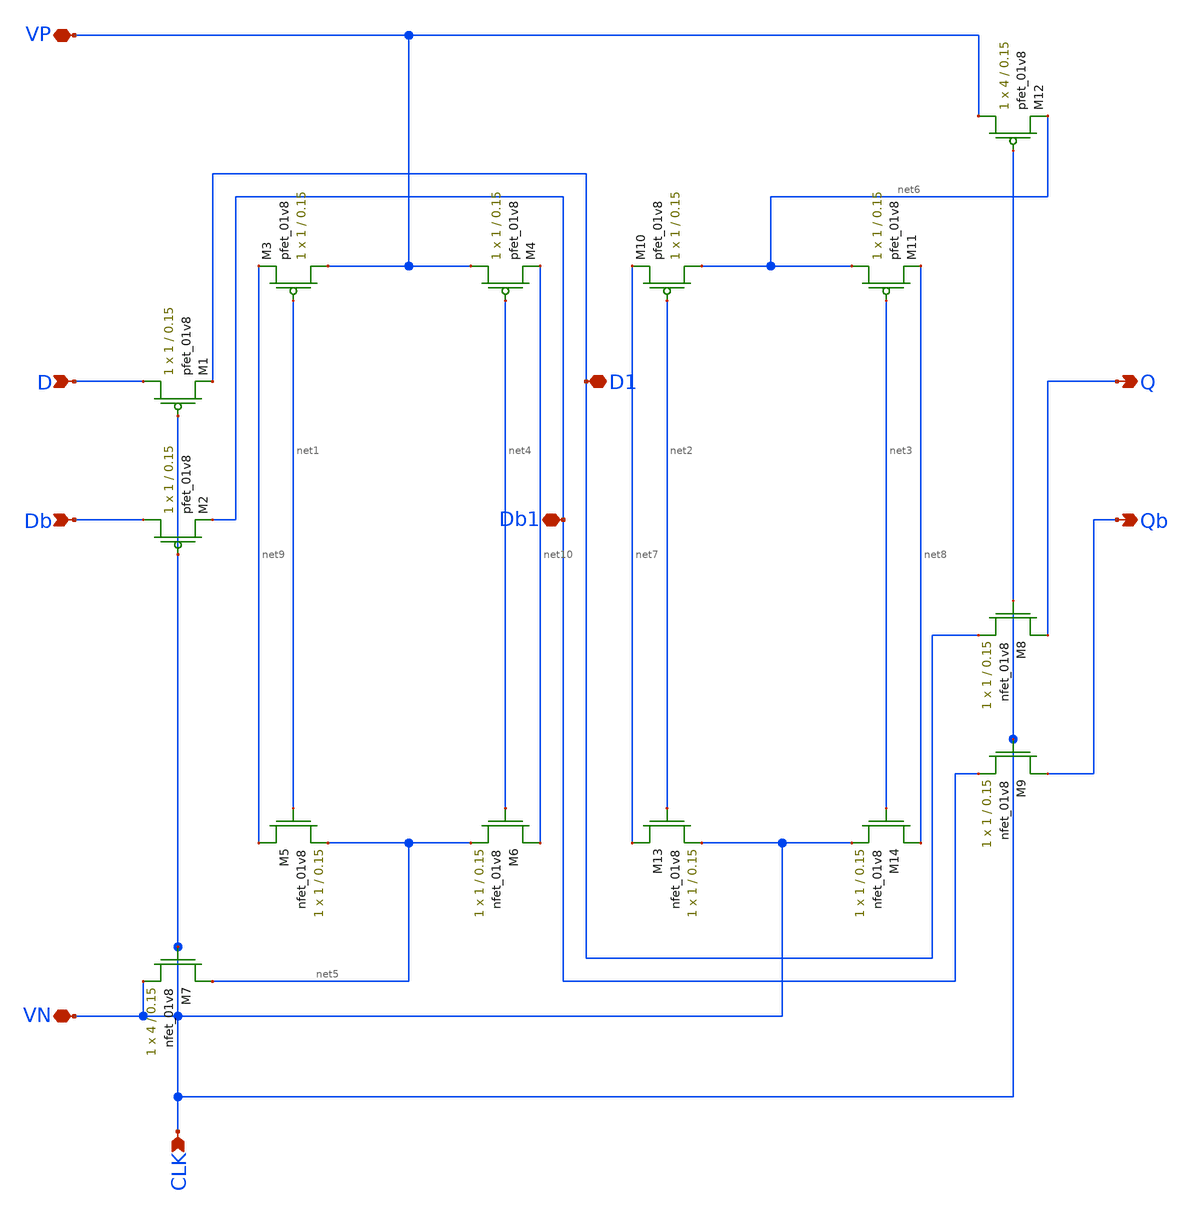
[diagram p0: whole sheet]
** sch_path: simulation/shift_register/andrew_mp2_files/d_flipflop/d_flipflop_LDS_v2.sch
**.subckt d_flipflop_LDS_v2 D CLK Q Qb Db VP VN D1 Db1
*.ipin D
*.ipin CLK
*.opin Q
*.opin Qb
*.ipin Db
*.iopin VP
*.iopin VN
*.iopin D1
*.iopin Db1
XM1 D CLK D1 VDD sky130_fd_pr__pfet_01v8 L=0.15 W=1 nf=1 ad='int((nf+1)/2) * W/nf * 0.29' as='int((nf+2)/2) * W/nf * 0.29'
+ pd='2*int((nf+1)/2) * (W/nf + 0.29)' ps='2*int((nf+2)/2) * (W/nf + 0.29)' nrd='0.29 / W' nrs='0.29 / W'
+ sa=0 sb=0 sd=0 mult=1 m=1
XM2 Db CLK Db1 VDD sky130_fd_pr__pfet_01v8 L=0.15 W=1 nf=1 ad='int((nf+1)/2) * W/nf * 0.29' as='int((nf+2)/2) * W/nf * 0.29'
+ pd='2*int((nf+1)/2) * (W/nf + 0.29)' ps='2*int((nf+2)/2) * (W/nf + 0.29)' nrd='0.29 / W' nrs='0.29 / W'
+ sa=0 sb=0 sd=0 mult=1 m=1
XM3 VP net1 net9 VDD sky130_fd_pr__pfet_01v8 L=0.15 W=1 nf=1 ad='int((nf+1)/2) * W/nf * 0.29' as='int((nf+2)/2) * W/nf * 0.29'
+ pd='2*int((nf+1)/2) * (W/nf + 0.29)' ps='2*int((nf+2)/2) * (W/nf + 0.29)' nrd='0.29 / W' nrs='0.29 / W'
+ sa=0 sb=0 sd=0 mult=1 m=1
XM5 net9 net1 net5 GND sky130_fd_pr__nfet_01v8 L=0.15 W=1 nf=1 ad='int((nf+1)/2) * W/nf * 0.29' as='int((nf+2)/2) * W/nf * 0.29'
+ pd='2*int((nf+1)/2) * (W/nf + 0.29)' ps='2*int((nf+2)/2) * (W/nf + 0.29)' nrd='0.29 / W' nrs='0.29 / W'
+ sa=0 sb=0 sd=0 mult=1 m=1
XM7 net5 CLK CLK GND sky130_fd_pr__nfet_01v8 L=0.15 W=4 nf=1 ad='int((nf+1)/2) * W/nf * 0.29' as='int((nf+2)/2) * W/nf * 0.29'
+ pd='2*int((nf+1)/2) * (W/nf + 0.29)' ps='2*int((nf+2)/2) * (W/nf + 0.29)' nrd='0.29 / W' nrs='0.29 / W'
+ sa=0 sb=0 sd=0 mult=1 m=1
XM8 Q CLK D1 GND sky130_fd_pr__nfet_01v8 L=0.15 W=1 nf=1 ad='int((nf+1)/2) * W/nf * 0.29' as='int((nf+2)/2) * W/nf * 0.29'
+ pd='2*int((nf+1)/2) * (W/nf + 0.29)' ps='2*int((nf+2)/2) * (W/nf + 0.29)' nrd='0.29 / W' nrs='0.29 / W'
+ sa=0 sb=0 sd=0 mult=1 m=1
XM9 Qb CLK Db1 GND sky130_fd_pr__nfet_01v8 L=0.15 W=1 nf=1 ad='int((nf+1)/2) * W/nf * 0.29' as='int((nf+2)/2) * W/nf * 0.29'
+ pd='2*int((nf+1)/2) * (W/nf + 0.29)' ps='2*int((nf+2)/2) * (W/nf + 0.29)' nrd='0.29 / W' nrs='0.29 / W'
+ sa=0 sb=0 sd=0 mult=1 m=1
XM10 net6 net2 net7 VDD sky130_fd_pr__pfet_01v8 L=0.15 W=1 nf=1 ad='int((nf+1)/2) * W/nf * 0.29' as='int((nf+2)/2) * W/nf * 0.29'
+ pd='2*int((nf+1)/2) * (W/nf + 0.29)' ps='2*int((nf+2)/2) * (W/nf + 0.29)' nrd='0.29 / W' nrs='0.29 / W'
+ sa=0 sb=0 sd=0 mult=1 m=1
XM11 net6 net3 net8 VDD sky130_fd_pr__pfet_01v8 L=0.15 W=1 nf=1 ad='int((nf+1)/2) * W/nf * 0.29' as='int((nf+2)/2) * W/nf * 0.29'
+ pd='2*int((nf+1)/2) * (W/nf + 0.29)' ps='2*int((nf+2)/2) * (W/nf + 0.29)' nrd='0.29 / W' nrs='0.29 / W'
+ sa=0 sb=0 sd=0 mult=1 m=1
XM12 VP CLK net6 VDD sky130_fd_pr__pfet_01v8 L=0.15 W=4 nf=1 ad='int((nf+1)/2) * W/nf * 0.29' as='int((nf+2)/2) * W/nf * 0.29'
+ pd='2*int((nf+1)/2) * (W/nf + 0.29)' ps='2*int((nf+2)/2) * (W/nf + 0.29)' nrd='0.29 / W' nrs='0.29 / W'
+ sa=0 sb=0 sd=0 mult=1 m=1
XM13 net7 net2 CLK GND sky130_fd_pr__nfet_01v8 L=0.15 W=1 nf=1 ad='int((nf+1)/2) * W/nf * 0.29' as='int((nf+2)/2) * W/nf * 0.29'
+ pd='2*int((nf+1)/2) * (W/nf + 0.29)' ps='2*int((nf+2)/2) * (W/nf + 0.29)' nrd='0.29 / W' nrs='0.29 / W'
+ sa=0 sb=0 sd=0 mult=1 m=1
XM14 net8 net3 CLK GND sky130_fd_pr__nfet_01v8 L=0.15 W=1 nf=1 ad='int((nf+1)/2) * W/nf * 0.29' as='int((nf+2)/2) * W/nf * 0.29'
+ pd='2*int((nf+1)/2) * (W/nf + 0.29)' ps='2*int((nf+2)/2) * (W/nf + 0.29)' nrd='0.29 / W' nrs='0.29 / W'
+ sa=0 sb=0 sd=0 mult=1 m=1
XM4 VP net4 net10 VDD sky130_fd_pr__pfet_01v8 L=0.15 W=1 nf=1 ad='int((nf+1)/2) * W/nf * 0.29' as='int((nf+2)/2) * W/nf * 0.29'
+ pd='2*int((nf+1)/2) * (W/nf + 0.29)' ps='2*int((nf+2)/2) * (W/nf + 0.29)' nrd='0.29 / W' nrs='0.29 / W'
+ sa=0 sb=0 sd=0 mult=1 m=1
XM6 net10 net4 net5 GND sky130_fd_pr__nfet_01v8 L=0.15 W=1 nf=1 ad='int((nf+1)/2) * W/nf * 0.29' as='int((nf+2)/2) * W/nf * 0.29'
+ pd='2*int((nf+1)/2) * (W/nf + 0.29)' ps='2*int((nf+2)/2) * (W/nf + 0.29)' nrd='0.29 / W' nrs='0.29 / W'
+ sa=0 sb=0 sd=0 mult=1 m=1
**.ends
.end
